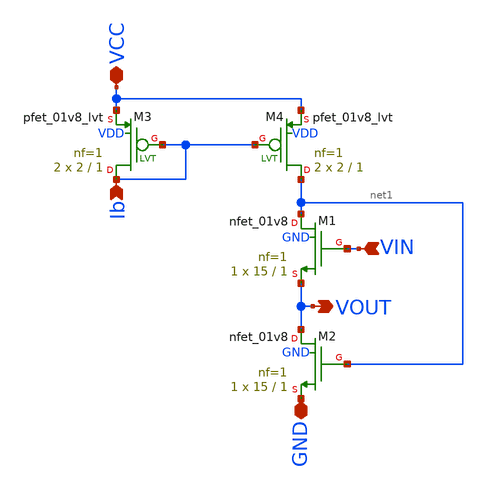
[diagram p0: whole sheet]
** sch_path: xschem/fvf.sch
**.subckt fvf VIN Ib VOUT VCC GND
*.ipin VIN
*.ipin Ib
*.opin VOUT
*.iopin VCC
*.iopin GND
XM1 net1 VIN VOUT GND sky130_fd_pr__nfet_01v8 L=1 W=15 nf=1 ad='int((nf+1)/2) * W/nf * 0.29' as='int((nf+2)/2) * W/nf * 0.29'
+ pd='2*int((nf+1)/2) * (W/nf + 0.29)' ps='2*int((nf+2)/2) * (W/nf + 0.29)' nrd='0.29 / W' nrs='0.29 / W'
+ sa=0 sb=0 sd=0 mult=1 m=1
XM2 VOUT net1 GND GND sky130_fd_pr__nfet_01v8 L=1 W=15 nf=1 ad='int((nf+1)/2) * W/nf * 0.29' as='int((nf+2)/2) * W/nf * 0.29'
+ pd='2*int((nf+1)/2) * (W/nf + 0.29)' ps='2*int((nf+2)/2) * (W/nf + 0.29)' nrd='0.29 / W' nrs='0.29 / W'
+ sa=0 sb=0 sd=0 mult=1 m=1
XM3 Ib Ib VCC VDD sky130_fd_pr__pfet_01v8_lvt L=1 W=2 nf=1 ad='int((nf+1)/2) * W/nf * 0.29' as='int((nf+2)/2) * W/nf * 0.29'
+ pd='2*int((nf+1)/2) * (W/nf + 0.29)' ps='2*int((nf+2)/2) * (W/nf + 0.29)' nrd='0.29 / W' nrs='0.29 / W'
+ sa=0 sb=0 sd=0 mult=2 m=2
XM4 net1 Ib VCC VDD sky130_fd_pr__pfet_01v8_lvt L=1 W=2 nf=1 ad='int((nf+1)/2) * W/nf * 0.29' as='int((nf+2)/2) * W/nf * 0.29'
+ pd='2*int((nf+1)/2) * (W/nf + 0.29)' ps='2*int((nf+2)/2) * (W/nf + 0.29)' nrd='0.29 / W' nrs='0.29 / W'
+ sa=0 sb=0 sd=0 mult=2 m=2
**.ends
.end
